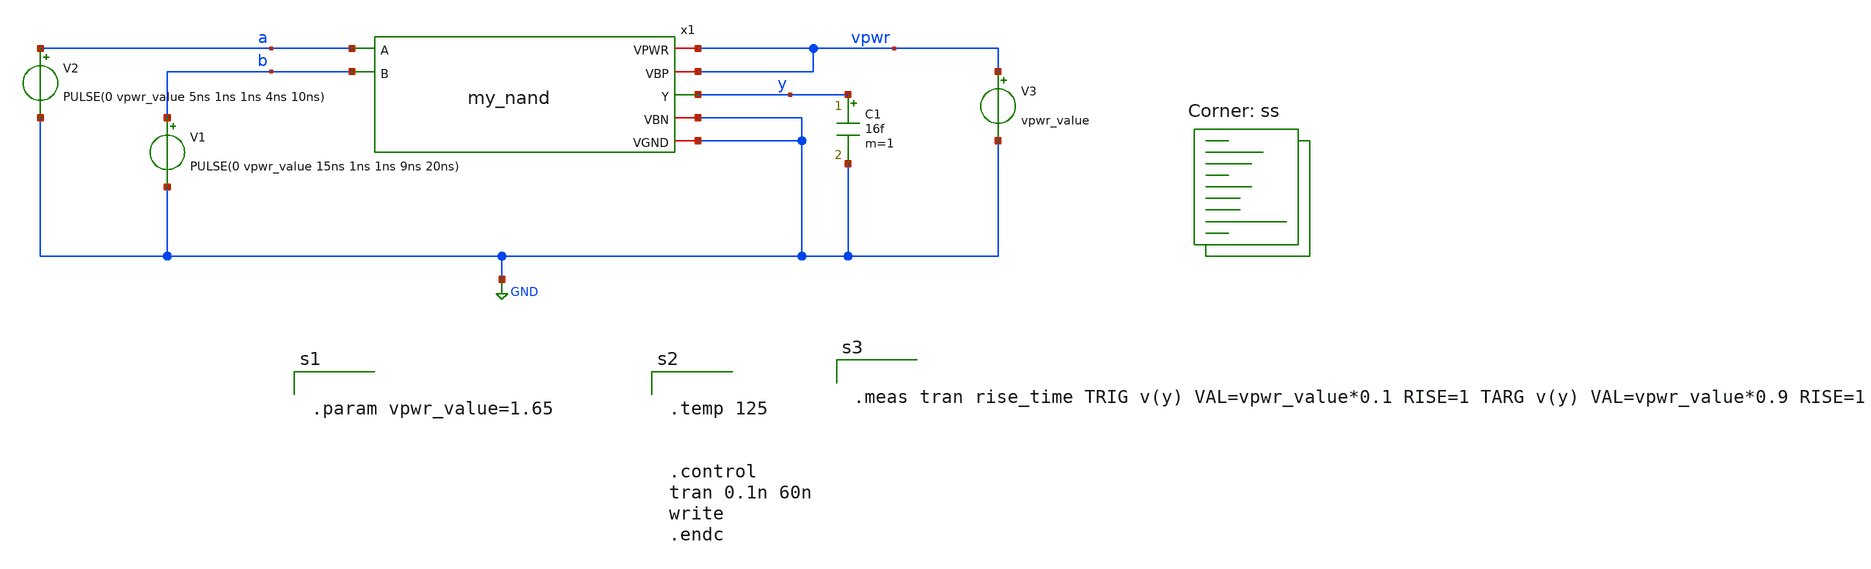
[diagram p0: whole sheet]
** sch_path: docs/_static/analog_flow_files/my_nand_tb.sch
**.subckt my_nand_tb
x1 vpwr vpwr a y GND b GND my_nand
V1 b GND PULSE(0 vpwr_value 15ns 1ns 1ns 9ns 20ns)
C1 y GND 16f m=1
V2 a GND PULSE(0 vpwr_value 5ns 1ns 1ns 4ns 10ns)
V3 vpwr GND vpwr_value
**** begin user architecture code


.param vpwr_value=1.65


.lib $::SKYWATER_MODELS/sky130.lib.spice ss


.temp 125


.control
tran 0.1n 60n
write
.endc





.meas tran rise_time TRIG v(y) VAL=vpwr_value*0.1 RISE=1 TARG v(y) VAL=vpwr_value*0.9 RISE=1


**** end user architecture code
**.ends

* expanding   symbol:  my_nand.sym # of pins=7
** sym_path: docs/_static/analog_flow_files/my_nand.sym
** sch_path: docs/_static/analog_flow_files/my_nand.sch
.subckt my_nand VPWR VBP A Y VBN B VGND
*.iopin VPWR
*.iopin VBP
*.iopin VBN
*.iopin VGND
*.ipin A
*.ipin B
*.opin Y
XM1 Y A net1 VBN sky130_fd_pr__nfet_01v8 L=0.15 W=0.65 nf=1 ad='int((nf+1)/2) * W/nf * 0.29' as='int((nf+2)/2) * W/nf * 0.29'
+ pd='2*int((nf+1)/2) * (W/nf + 0.29)' ps='2*int((nf+2)/2) * (W/nf + 0.29)' nrd='0.29 / W' nrs='0.29 / W'
+ sa=0 sb=0 sd=0 mult=1 m=1
XM2 Y A VPWR VBP sky130_fd_pr__pfet_01v8 L=0.15 W=1 nf=1 ad='int((nf+1)/2) * W/nf * 0.29' as='int((nf+2)/2) * W/nf * 0.29'
+ pd='2*int((nf+1)/2) * (W/nf + 0.29)' ps='2*int((nf+2)/2) * (W/nf + 0.29)' nrd='0.29 / W' nrs='0.29 / W'
+ sa=0 sb=0 sd=0 mult=1 m=1
XM3 VPWR B Y VBP sky130_fd_pr__pfet_01v8 L=0.15 W=1 nf=1 ad='int((nf+1)/2) * W/nf * 0.29' as='int((nf+2)/2) * W/nf * 0.29'
+ pd='2*int((nf+1)/2) * (W/nf + 0.29)' ps='2*int((nf+2)/2) * (W/nf + 0.29)' nrd='0.29 / W' nrs='0.29 / W'
+ sa=0 sb=0 sd=0 mult=1 m=1
XM4 net1 B VGND VBN sky130_fd_pr__nfet_01v8 L=0.15 W=0.65 nf=1 ad='int((nf+1)/2) * W/nf * 0.29' as='int((nf+2)/2) * W/nf * 0.29'
+ pd='2*int((nf+1)/2) * (W/nf + 0.29)' ps='2*int((nf+2)/2) * (W/nf + 0.29)' nrd='0.29 / W' nrs='0.29 / W'
+ sa=0 sb=0 sd=0 mult=1 m=1
.ends

.GLOBAL GND
.end
